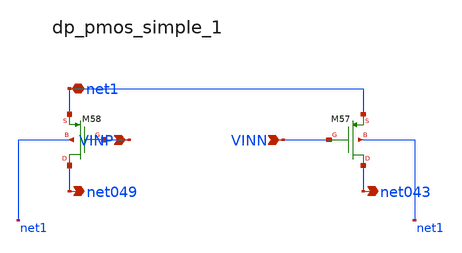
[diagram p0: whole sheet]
** sch_path: analog-db/raw/amp_016_song_dacfc/hier/blocks/dp_pmos_simple_1.sch
**.subckt dp_pmos_simple_1 VINP VINN net1 net049 net043
*.ipin VINP
*.ipin VINN
*.iopin net1
*.opin net049
*.opin net043
XM57 net043 VINN net1 net1 sg13_lv_pmos w=x_dut_xm57_w l=x_dut_xm57_l ng=1 m=x_dut_xm57_m
XM58 net049 VINP net1 net1 sg13_lv_pmos w=x_dut_xm58_w l=x_dut_xm58_l ng=1 m=x_dut_xm58_m
**.ends
.end
